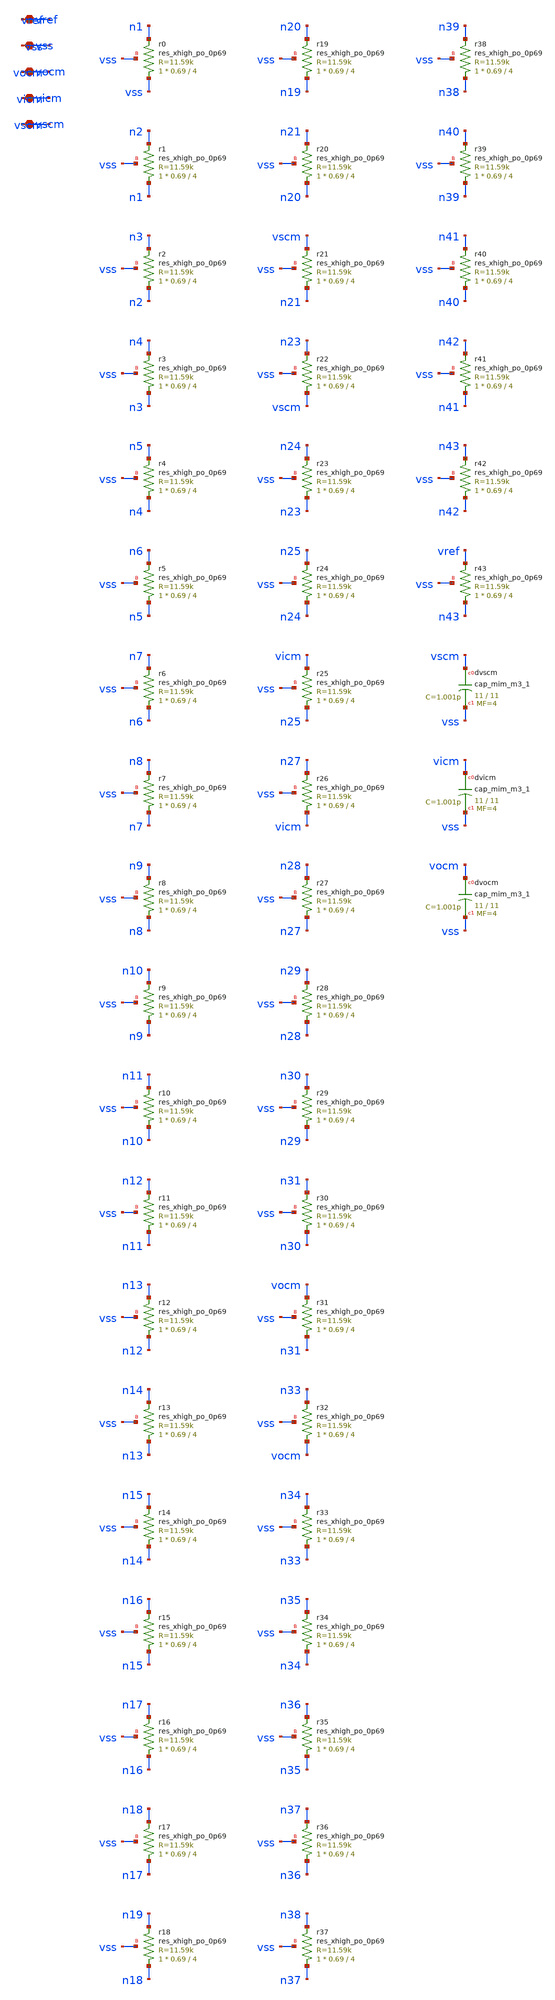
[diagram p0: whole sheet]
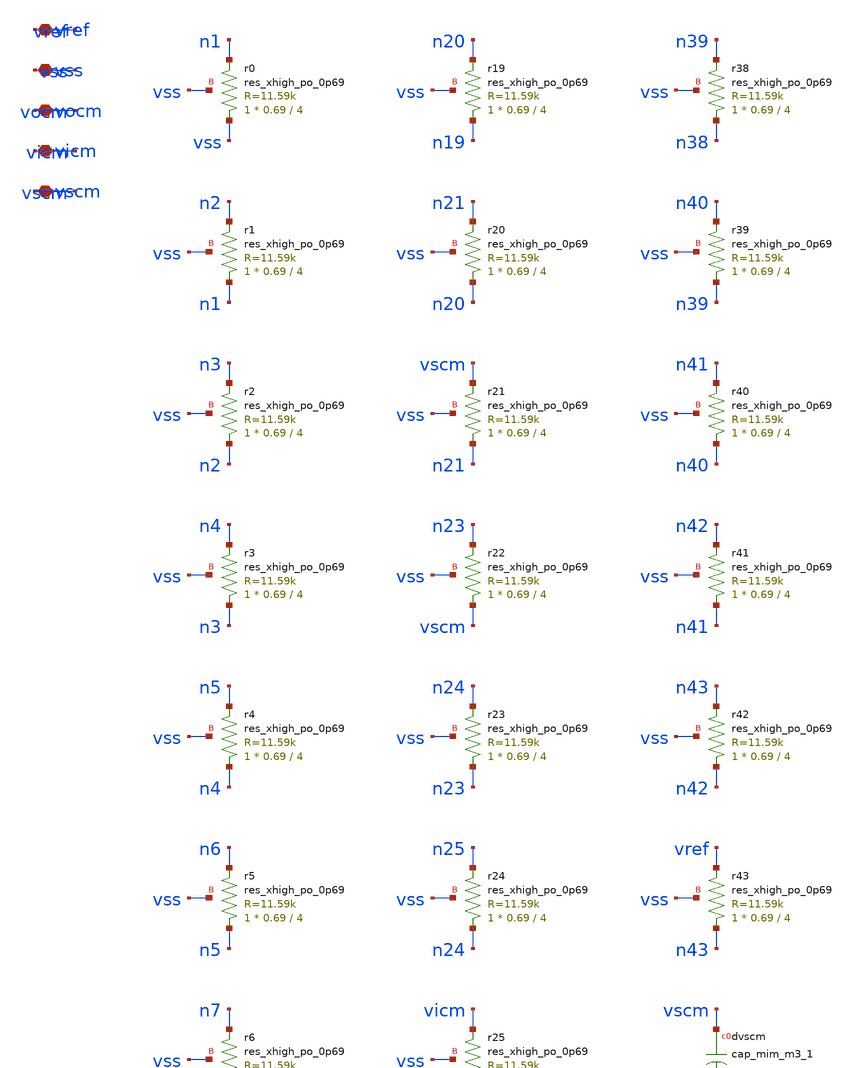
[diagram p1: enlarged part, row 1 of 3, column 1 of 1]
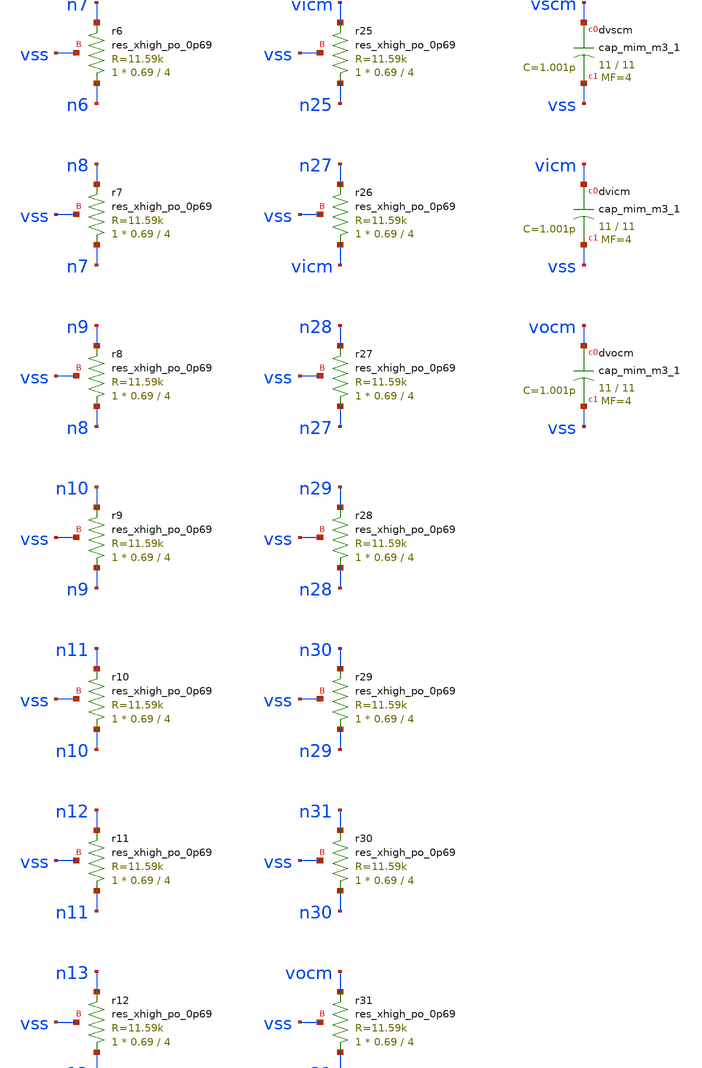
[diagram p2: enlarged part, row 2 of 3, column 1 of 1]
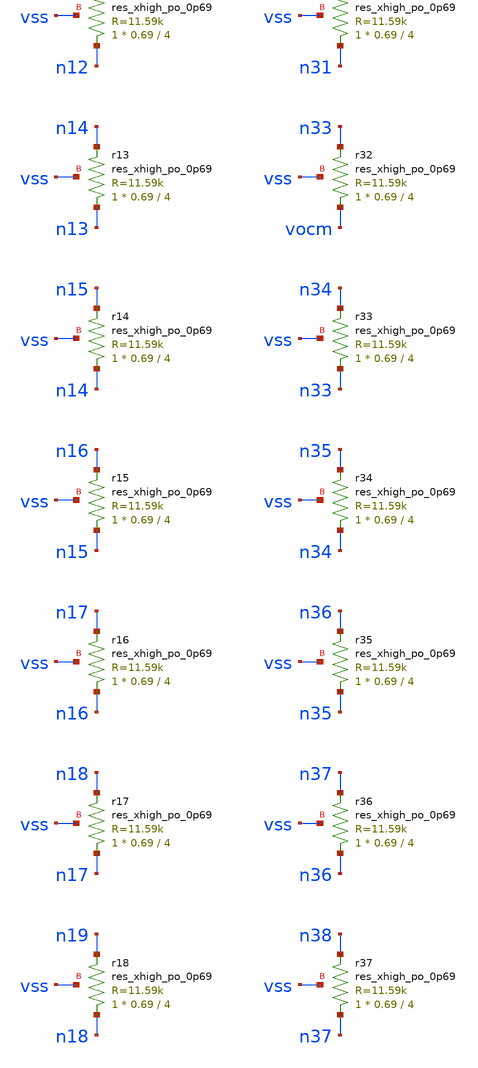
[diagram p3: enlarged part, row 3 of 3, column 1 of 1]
** sch_path: design/xschem/sch/c5c7_ref.sch
**.subckt c5c7_ref vref vss vocm vicm vscm
*.iopin vref
*.iopin vss
*.iopin vocm
*.iopin vicm
*.iopin vscm
Xr0 vss n1 vss sky130_fd_pr__res_xhigh_po_0p69 L=4 mult=1 m=1
Xr1 n1 n2 vss sky130_fd_pr__res_xhigh_po_0p69 L=4 mult=1 m=1
Xr2 n2 n3 vss sky130_fd_pr__res_xhigh_po_0p69 L=4 mult=1 m=1
Xr3 n3 n4 vss sky130_fd_pr__res_xhigh_po_0p69 L=4 mult=1 m=1
Xr4 n4 n5 vss sky130_fd_pr__res_xhigh_po_0p69 L=4 mult=1 m=1
Xr5 n5 n6 vss sky130_fd_pr__res_xhigh_po_0p69 L=4 mult=1 m=1
Xr6 n6 n7 vss sky130_fd_pr__res_xhigh_po_0p69 L=4 mult=1 m=1
Xr7 n7 n8 vss sky130_fd_pr__res_xhigh_po_0p69 L=4 mult=1 m=1
Xr8 n8 n9 vss sky130_fd_pr__res_xhigh_po_0p69 L=4 mult=1 m=1
Xr9 n9 n10 vss sky130_fd_pr__res_xhigh_po_0p69 L=4 mult=1 m=1
Xr10 n10 n11 vss sky130_fd_pr__res_xhigh_po_0p69 L=4 mult=1 m=1
Xr11 n11 n12 vss sky130_fd_pr__res_xhigh_po_0p69 L=4 mult=1 m=1
Xr12 n12 n13 vss sky130_fd_pr__res_xhigh_po_0p69 L=4 mult=1 m=1
Xr13 n13 n14 vss sky130_fd_pr__res_xhigh_po_0p69 L=4 mult=1 m=1
Xr14 n14 n15 vss sky130_fd_pr__res_xhigh_po_0p69 L=4 mult=1 m=1
Xr15 n15 n16 vss sky130_fd_pr__res_xhigh_po_0p69 L=4 mult=1 m=1
Xr16 n16 n17 vss sky130_fd_pr__res_xhigh_po_0p69 L=4 mult=1 m=1
Xr17 n17 n18 vss sky130_fd_pr__res_xhigh_po_0p69 L=4 mult=1 m=1
Xr18 n18 n19 vss sky130_fd_pr__res_xhigh_po_0p69 L=4 mult=1 m=1
Xr19 n19 n20 vss sky130_fd_pr__res_xhigh_po_0p69 L=4 mult=1 m=1
Xr20 n20 n21 vss sky130_fd_pr__res_xhigh_po_0p69 L=4 mult=1 m=1
Xr21 n21 vscm vss sky130_fd_pr__res_xhigh_po_0p69 L=4 mult=1 m=1
Xr22 vscm n23 vss sky130_fd_pr__res_xhigh_po_0p69 L=4 mult=1 m=1
Xr23 n23 n24 vss sky130_fd_pr__res_xhigh_po_0p69 L=4 mult=1 m=1
Xr24 n24 n25 vss sky130_fd_pr__res_xhigh_po_0p69 L=4 mult=1 m=1
Xr25 n25 vicm vss sky130_fd_pr__res_xhigh_po_0p69 L=4 mult=1 m=1
Xr26 vicm n27 vss sky130_fd_pr__res_xhigh_po_0p69 L=4 mult=1 m=1
Xr27 n27 n28 vss sky130_fd_pr__res_xhigh_po_0p69 L=4 mult=1 m=1
Xr28 n28 n29 vss sky130_fd_pr__res_xhigh_po_0p69 L=4 mult=1 m=1
Xr29 n29 n30 vss sky130_fd_pr__res_xhigh_po_0p69 L=4 mult=1 m=1
Xr30 n30 n31 vss sky130_fd_pr__res_xhigh_po_0p69 L=4 mult=1 m=1
Xr31 n31 vocm vss sky130_fd_pr__res_xhigh_po_0p69 L=4 mult=1 m=1
Xr32 vocm n33 vss sky130_fd_pr__res_xhigh_po_0p69 L=4 mult=1 m=1
Xr33 n33 n34 vss sky130_fd_pr__res_xhigh_po_0p69 L=4 mult=1 m=1
Xr34 n34 n35 vss sky130_fd_pr__res_xhigh_po_0p69 L=4 mult=1 m=1
Xr35 n35 n36 vss sky130_fd_pr__res_xhigh_po_0p69 L=4 mult=1 m=1
Xr36 n36 n37 vss sky130_fd_pr__res_xhigh_po_0p69 L=4 mult=1 m=1
Xr37 n37 n38 vss sky130_fd_pr__res_xhigh_po_0p69 L=4 mult=1 m=1
Xr38 n38 n39 vss sky130_fd_pr__res_xhigh_po_0p69 L=4 mult=1 m=1
Xr39 n39 n40 vss sky130_fd_pr__res_xhigh_po_0p69 L=4 mult=1 m=1
Xr40 n40 n41 vss sky130_fd_pr__res_xhigh_po_0p69 L=4 mult=1 m=1
Xr41 n41 n42 vss sky130_fd_pr__res_xhigh_po_0p69 L=4 mult=1 m=1
Xr42 n42 n43 vss sky130_fd_pr__res_xhigh_po_0p69 L=4 mult=1 m=1
Xr43 n43 vref vss sky130_fd_pr__res_xhigh_po_0p69 L=4 mult=1 m=1
Xdvscm vscm vss sky130_fd_pr__cap_mim_m3_1 W=11 L=11 MF=4 m=4
Xdvicm vicm vss sky130_fd_pr__cap_mim_m3_1 W=11 L=11 MF=4 m=4
Xdvocm vocm vss sky130_fd_pr__cap_mim_m3_1 W=11 L=11 MF=4 m=4
**.ends
.end
